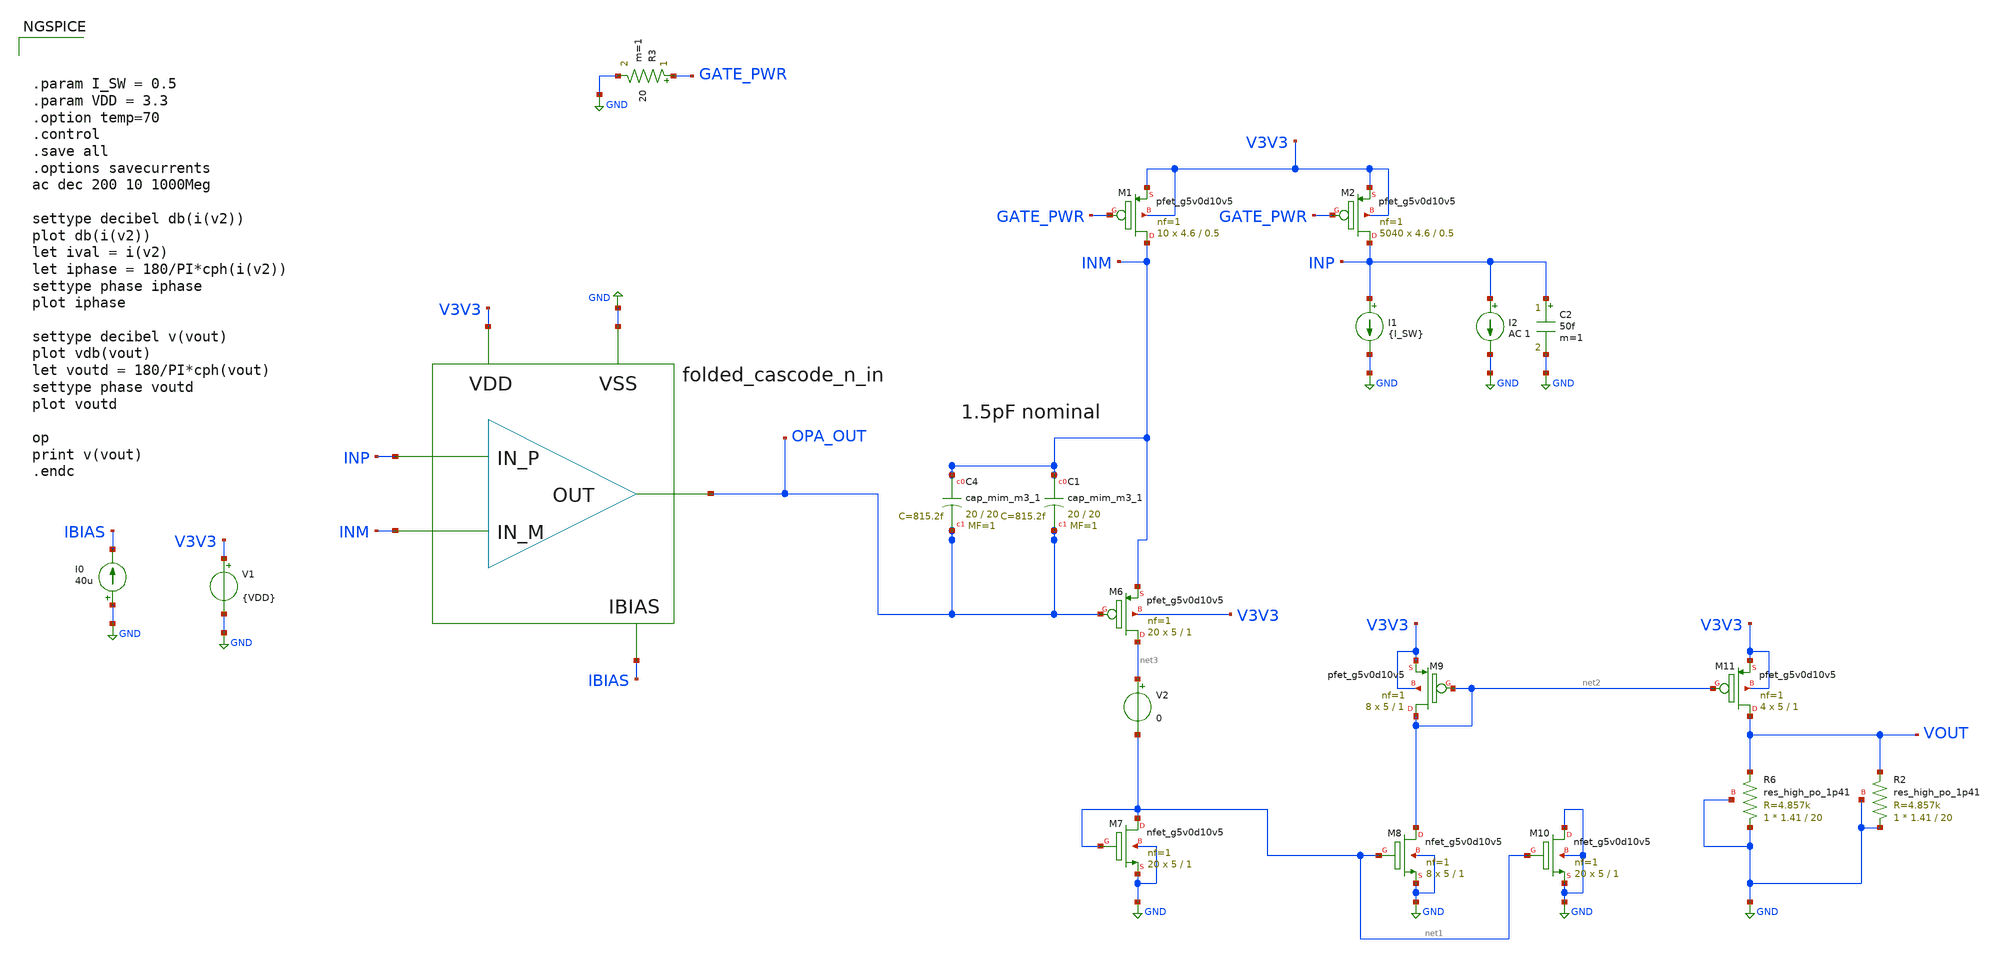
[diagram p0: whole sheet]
** sch_path: images/foss-asic-tools/addons/examples/open-pmic/design/current-sense/current_sense_ac.sch
**.subckt current_sense_ac
V1 V3V3 GND {VDD}
I0 GND IBIAS 40u
x1 INP INM OPA_OUT V3V3 GND IBIAS folded_cascode_n_in
XM1 INM GATE_PWR V3V3 V3V3 sky130_fd_pr__pfet_g5v0d10v5 L=0.5 W=4.6 nf=1 ad='int((nf+1)/2) * W/nf * 0.29'
+ as='int((nf+2)/2) * W/nf * 0.29' pd='2*int((nf+1)/2) * (W/nf + 0.29)' ps='2*int((nf+2)/2) * (W/nf + 0.29)'
+ nrd='0.29 / W' nrs='0.29 / W' sa=0 sb=0 sd=0 mult=10 m=10
XM2 INP GATE_PWR V3V3 V3V3 sky130_fd_pr__pfet_g5v0d10v5 L=0.5 W=4.6 nf=1 ad='int((nf+1)/2) * W/nf * 0.29'
+ as='int((nf+2)/2) * W/nf * 0.29' pd='2*int((nf+1)/2) * (W/nf + 0.29)' ps='2*int((nf+2)/2) * (W/nf + 0.29)'
+ nrd='0.29 / W' nrs='0.29 / W' sa=0 sb=0 sd=0 mult=5040 m=5040
R3 GATE_PWR GND 20 m=1
I1 INP GND {I_SW}
I2 INP GND AC 1
C2 INP GND 50f m=1
XM6 net3 OPA_OUT INM V3V3 sky130_fd_pr__pfet_g5v0d10v5 L=1 W=5 nf=1 ad='int((nf+1)/2) * W/nf * 0.29'
+ as='int((nf+2)/2) * W/nf * 0.29' pd='2*int((nf+1)/2) * (W/nf + 0.29)' ps='2*int((nf+2)/2) * (W/nf + 0.29)'
+ nrd='0.29 / W' nrs='0.29 / W' sa=0 sb=0 sd=0 mult=20 m=20
XM7 net1 net1 GND GND sky130_fd_pr__nfet_g5v0d10v5 L=1 W=5 nf=1 ad='int((nf+1)/2) * W/nf * 0.29' as='int((nf+2)/2) * W/nf * 0.29'
+ pd='2*int((nf+1)/2) * (W/nf + 0.29)' ps='2*int((nf+2)/2) * (W/nf + 0.29)' nrd='0.29 / W' nrs='0.29 / W'
+ sa=0 sb=0 sd=0 mult=20 m=20
XM8 net2 net1 GND GND sky130_fd_pr__nfet_g5v0d10v5 L=1 W=5 nf=1 ad='int((nf+1)/2) * W/nf * 0.29' as='int((nf+2)/2) * W/nf * 0.29'
+ pd='2*int((nf+1)/2) * (W/nf + 0.29)' ps='2*int((nf+2)/2) * (W/nf + 0.29)' nrd='0.29 / W' nrs='0.29 / W'
+ sa=0 sb=0 sd=0 mult=8 m=8
XM9 net2 net2 V3V3 V3V3 sky130_fd_pr__pfet_g5v0d10v5 L=1 W=5 nf=1 ad='int((nf+1)/2) * W/nf * 0.29' as='int((nf+2)/2) * W/nf * 0.29'
+ pd='2*int((nf+1)/2) * (W/nf + 0.29)' ps='2*int((nf+2)/2) * (W/nf + 0.29)' nrd='0.29 / W' nrs='0.29 / W'
+ sa=0 sb=0 sd=0 mult=8 m=8
XM10 GND net1 GND GND sky130_fd_pr__nfet_g5v0d10v5 L=1 W=5 nf=1 ad='int((nf+1)/2) * W/nf * 0.29' as='int((nf+2)/2) * W/nf * 0.29'
+ pd='2*int((nf+1)/2) * (W/nf + 0.29)' ps='2*int((nf+2)/2) * (W/nf + 0.29)' nrd='0.29 / W' nrs='0.29 / W'
+ sa=0 sb=0 sd=0 mult=20 m=20
XM11 VOUT net2 V3V3 V3V3 sky130_fd_pr__pfet_g5v0d10v5 L=1 W=5 nf=1 ad='int((nf+1)/2) * W/nf * 0.29' as='int((nf+2)/2) * W/nf * 0.29'
+ pd='2*int((nf+1)/2) * (W/nf + 0.29)' ps='2*int((nf+2)/2) * (W/nf + 0.29)' nrd='0.29 / W' nrs='0.29 / W'
+ sa=0 sb=0 sd=0 mult=4 m=4
XR6 GND VOUT GND sky130_fd_pr__res_high_po_1p41 L=20 mult=1 m=1
XR2 GND VOUT GND sky130_fd_pr__res_high_po_1p41 L=20 mult=1 m=1
V2 net3 net1 0
XC4 INM OPA_OUT sky130_fd_pr__cap_mim_m3_1 W=20 L=20 MF=1 m=1
XC1 INM OPA_OUT sky130_fd_pr__cap_mim_m3_1 W=20 L=20 MF=1 m=1
**** begin user architecture code



.param I_SW = 0.5
.param VDD = 3.3
.option temp=70
.control
.save all
.options savecurrents
ac dec 200 10 1000Meg

settype decibel db(i(v2))
plot db(i(v2))
let ival = i(v2)
let iphase = 180/PI*cph(i(v2))
settype phase iphase
plot iphase

settype decibel v(vout)
plot vdb(vout)
let voutd = 180/PI*cph(vout)
settype phase voutd
plot voutd

op
print v(vout)
.endc



.lib $::SKYWATER_MODELS/models/sky130.lib.spice tt
.option wnflag=1

**** end user architecture code
**.ends
.GLOBAL GND
**** begin user architecture code
[sky130_models]
**** end user architecture code
.end
